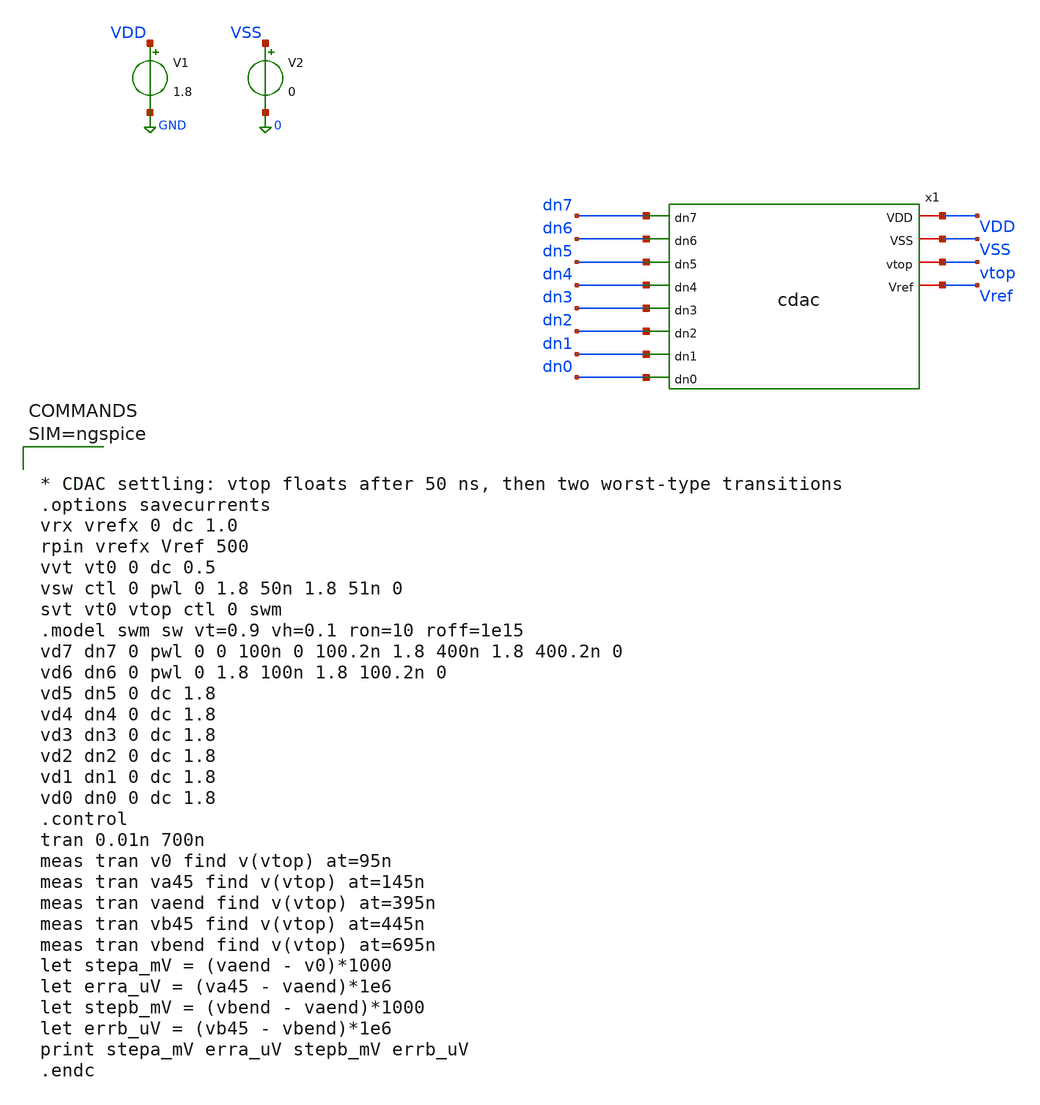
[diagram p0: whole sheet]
** sch_path: xschem/cdac_tb.sch
**.subckt cdac_tb
V1 VDD GND 1.8
V2 VSS 0 0
x1 VDD dn7 dn6 dn5 VSS dn4 dn3 vtop dn2 dn1 Vref dn0 cdac
**** begin user architecture code

** opencircuitdesign pdks install
.lib $::SKYWATER_MODELS/sky130.lib.spice tt




* CDAC settling: vtop floats after 50 ns, then two worst-type transitions
.options savecurrents
vrx vrefx 0 dc 1.0
rpin vrefx Vref 500
vvt vt0 0 dc 0.5
vsw ctl 0 pwl 0 1.8 50n 1.8 51n 0
svt vt0 vtop ctl 0 swm
.model swm sw vt=0.9 vh=0.1 ron=10 roff=1e15
vd7 dn7 0 pwl 0 0 100n 0 100.2n 1.8 400n 1.8 400.2n 0
vd6 dn6 0 pwl 0 1.8 100n 1.8 100.2n 0
vd5 dn5 0 dc 1.8
vd4 dn4 0 dc 1.8
vd3 dn3 0 dc 1.8
vd2 dn2 0 dc 1.8
vd1 dn1 0 dc 1.8
vd0 dn0 0 dc 1.8
.control
tran 0.01n 700n
meas tran v0 find v(vtop) at=95n
meas tran va45 find v(vtop) at=145n
meas tran vaend find v(vtop) at=395n
meas tran vb45 find v(vtop) at=445n
meas tran vbend find v(vtop) at=695n
let stepa_mV = (vaend - v0)*1000
let erra_uV = (va45 - vaend)*1e6
let stepb_mV = (vbend - vaend)*1000
let errb_uV = (vb45 - vbend)*1e6
print stepa_mV erra_uV stepb_mV errb_uV
.endc



**** end user architecture code
**.ends

* expanding   symbol:  cdac.sym # of pins=12
** sym_path: xschem/cdac.sym
** sch_path: xschem/cdac.sch
.subckt cdac VDD dn7 dn6 dn5 VSS dn4 dn3 vtop dn2 dn1 Vref dn0
*.ipin dn7
*.ipin dn6
*.ipin dn5
*.ipin dn4
*.ipin dn3
*.ipin dn2
*.ipin dn1
*.ipin dn0
*.iopin VDD
*.iopin VSS
*.iopin vtop
*.iopin Vref
XMN7 b7 dn7 VSS VSS sky130_fd_pr__nfet_01v8 L=0.15 W=2 nf=1 ad='int((1 + 1)/2) * 2 / 1 * 0.29' as='int((1 + 2)/2) * 2 / 1 * 0.29'
+ pd='2*int((1 + 1)/2) * (2 / 1 + 0.29)' ps='2*int((1 + 2)/2) * (2 / 1 + 0.29)' nrd='0.29 / 2 ' nrs='0.29 / 2 '
+ sa=0 sb=0 sd=0 mult=1 m=1
XMP7 b7 dn7 Vref Vref sky130_fd_pr__pfet_01v8_lvt L=0.35 W=4 nf=1 ad='int((1 + 1)/2) * 4 / 1 * 0.29'
+ as='int((1 + 2)/2) * 4 / 1 * 0.29' pd='2*int((1 + 1)/2) * (4 / 1 + 0.29)' ps='2*int((1 + 2)/2) * (4 / 1 + 0.29)'
+ nrd='0.29 / 4 ' nrs='0.29 / 4 ' sa=0 sb=0 sd=0 mult=1 m=1
XC7 vtop b7 sky130_fd_pr__cap_mim_m3_1 W=1.8 L=1.8 MF=128 m=128
XMN6 b6 dn6 VSS VSS sky130_fd_pr__nfet_01v8 L=0.15 W=1 nf=1 ad='int((1 + 1)/2) * 1 / 1 * 0.29' as='int((1 + 2)/2) * 1 / 1 * 0.29'
+ pd='2*int((1 + 1)/2) * (1 / 1 + 0.29)' ps='2*int((1 + 2)/2) * (1 / 1 + 0.29)' nrd='0.29 / 1 ' nrs='0.29 / 1 '
+ sa=0 sb=0 sd=0 mult=1 m=1
XMP6 b6 dn6 Vref Vref sky130_fd_pr__pfet_01v8_lvt L=0.35 W=2 nf=1 ad='int((1 + 1)/2) * 2 / 1 * 0.29'
+ as='int((1 + 2)/2) * 2 / 1 * 0.29' pd='2*int((1 + 1)/2) * (2 / 1 + 0.29)' ps='2*int((1 + 2)/2) * (2 / 1 + 0.29)'
+ nrd='0.29 / 2 ' nrs='0.29 / 2 ' sa=0 sb=0 sd=0 mult=1 m=1
XC6 vtop b6 sky130_fd_pr__cap_mim_m3_1 W=1.8 L=1.8 MF=64 m=64
XMN5 b5 dn5 VSS VSS sky130_fd_pr__nfet_01v8 L=0.15 W=0.5 nf=1 ad='int((1 + 1)/2) * 0.5 / 1 * 0.29' as='int((1 + 2)/2) * 0.5 / 1 * 0.29'
+ pd='2*int((1 + 1)/2) * (0.5 / 1 + 0.29)' ps='2*int((1 + 2)/2) * (0.5 / 1 + 0.29)' nrd='0.29 / 0.5 ' nrs='0.29 / 0.5 '
+ sa=0 sb=0 sd=0 mult=1 m=1
XMP5 b5 dn5 Vref Vref sky130_fd_pr__pfet_01v8_lvt L=0.35 W=1 nf=1 ad='int((1 + 1)/2) * 1 / 1 * 0.29'
+ as='int((1 + 2)/2) * 1 / 1 * 0.29' pd='2*int((1 + 1)/2) * (1 / 1 + 0.29)' ps='2*int((1 + 2)/2) * (1 / 1 + 0.29)'
+ nrd='0.29 / 1 ' nrs='0.29 / 1 ' sa=0 sb=0 sd=0 mult=1 m=1
XC5 vtop b5 sky130_fd_pr__cap_mim_m3_1 W=1.8 L=1.8 MF=32 m=32
XMN4 b4 dn4 VSS VSS sky130_fd_pr__nfet_01v8 L=0.15 W=0.5 nf=1 ad='int((1 + 1)/2) * 0.5 / 1 * 0.29' as='int((1 + 2)/2) * 0.5 / 1 * 0.29'
+ pd='2*int((1 + 1)/2) * (0.5 / 1 + 0.29)' ps='2*int((1 + 2)/2) * (0.5 / 1 + 0.29)' nrd='0.29 / 0.5 ' nrs='0.29 / 0.5 '
+ sa=0 sb=0 sd=0 mult=1 m=1
XMP4 b4 dn4 Vref Vref sky130_fd_pr__pfet_01v8_lvt L=0.35 W=1 nf=1 ad='int((1 + 1)/2) * 1 / 1 * 0.29'
+ as='int((1 + 2)/2) * 1 / 1 * 0.29' pd='2*int((1 + 1)/2) * (1 / 1 + 0.29)' ps='2*int((1 + 2)/2) * (1 / 1 + 0.29)'
+ nrd='0.29 / 1 ' nrs='0.29 / 1 ' sa=0 sb=0 sd=0 mult=1 m=1
XC4 vtop b4 sky130_fd_pr__cap_mim_m3_1 W=1.8 L=1.8 MF=16 m=16
XMN3 b3 dn3 VSS VSS sky130_fd_pr__nfet_01v8 L=0.15 W=0.5 nf=1 ad='int((1 + 1)/2) * 0.5 / 1 * 0.29' as='int((1 + 2)/2) * 0.5 / 1 * 0.29'
+ pd='2*int((1 + 1)/2) * (0.5 / 1 + 0.29)' ps='2*int((1 + 2)/2) * (0.5 / 1 + 0.29)' nrd='0.29 / 0.5 ' nrs='0.29 / 0.5 '
+ sa=0 sb=0 sd=0 mult=1 m=1
XMP3 b3 dn3 Vref Vref sky130_fd_pr__pfet_01v8_lvt L=0.35 W=1 nf=1 ad='int((1 + 1)/2) * 1 / 1 * 0.29'
+ as='int((1 + 2)/2) * 1 / 1 * 0.29' pd='2*int((1 + 1)/2) * (1 / 1 + 0.29)' ps='2*int((1 + 2)/2) * (1 / 1 + 0.29)'
+ nrd='0.29 / 1 ' nrs='0.29 / 1 ' sa=0 sb=0 sd=0 mult=1 m=1
XC3 vtop b3 sky130_fd_pr__cap_mim_m3_1 W=1.8 L=1.8 MF=8 m=8
XMN2 b2 dn2 VSS VSS sky130_fd_pr__nfet_01v8 L=0.15 W=0.5 nf=1 ad='int((1 + 1)/2) * 0.5 / 1 * 0.29' as='int((1 + 2)/2) * 0.5 / 1 * 0.29'
+ pd='2*int((1 + 1)/2) * (0.5 / 1 + 0.29)' ps='2*int((1 + 2)/2) * (0.5 / 1 + 0.29)' nrd='0.29 / 0.5 ' nrs='0.29 / 0.5 '
+ sa=0 sb=0 sd=0 mult=1 m=1
XMP2 b2 dn2 Vref Vref sky130_fd_pr__pfet_01v8_lvt L=0.35 W=1 nf=1 ad='int((1 + 1)/2) * 1 / 1 * 0.29'
+ as='int((1 + 2)/2) * 1 / 1 * 0.29' pd='2*int((1 + 1)/2) * (1 / 1 + 0.29)' ps='2*int((1 + 2)/2) * (1 / 1 + 0.29)'
+ nrd='0.29 / 1 ' nrs='0.29 / 1 ' sa=0 sb=0 sd=0 mult=1 m=1
XC2 vtop b2 sky130_fd_pr__cap_mim_m3_1 W=1.8 L=1.8 MF=4 m=4
XMN1 b1 dn1 VSS VSS sky130_fd_pr__nfet_01v8 L=0.15 W=0.5 nf=1 ad='int((1 + 1)/2) * 0.5 / 1 * 0.29' as='int((1 + 2)/2) * 0.5 / 1 * 0.29'
+ pd='2*int((1 + 1)/2) * (0.5 / 1 + 0.29)' ps='2*int((1 + 2)/2) * (0.5 / 1 + 0.29)' nrd='0.29 / 0.5 ' nrs='0.29 / 0.5 '
+ sa=0 sb=0 sd=0 mult=1 m=1
XMP1 b1 dn1 Vref Vref sky130_fd_pr__pfet_01v8_lvt L=0.35 W=1 nf=1 ad='int((1 + 1)/2) * 1 / 1 * 0.29'
+ as='int((1 + 2)/2) * 1 / 1 * 0.29' pd='2*int((1 + 1)/2) * (1 / 1 + 0.29)' ps='2*int((1 + 2)/2) * (1 / 1 + 0.29)'
+ nrd='0.29 / 1 ' nrs='0.29 / 1 ' sa=0 sb=0 sd=0 mult=1 m=1
XC1 vtop b1 sky130_fd_pr__cap_mim_m3_1 W=1.8 L=1.8 MF=2 m=2
XMN0 b0 dn0 VSS VSS sky130_fd_pr__nfet_01v8 L=0.15 W=0.5 nf=1 ad='int((1 + 1)/2) * 0.5 / 1 * 0.29' as='int((1 + 2)/2) * 0.5 / 1 * 0.29'
+ pd='2*int((1 + 1)/2) * (0.5 / 1 + 0.29)' ps='2*int((1 + 2)/2) * (0.5 / 1 + 0.29)' nrd='0.29 / 0.5 ' nrs='0.29 / 0.5 '
+ sa=0 sb=0 sd=0 mult=1 m=1
XMP0 b0 dn0 Vref Vref sky130_fd_pr__pfet_01v8_lvt L=0.35 W=1 nf=1 ad='int((1 + 1)/2) * 1 / 1 * 0.29'
+ as='int((1 + 2)/2) * 1 / 1 * 0.29' pd='2*int((1 + 1)/2) * (1 / 1 + 0.29)' ps='2*int((1 + 2)/2) * (1 / 1 + 0.29)'
+ nrd='0.29 / 1 ' nrs='0.29 / 1 ' sa=0 sb=0 sd=0 mult=1 m=1
XC0 vtop b0 sky130_fd_pr__cap_mim_m3_1 W=1.8 L=1.8 MF=1 m=1
XCdmy vtop VSS sky130_fd_pr__cap_mim_m3_1 W=1.8 L=1.8 MF=1 m=1
.ends

.GLOBAL GND
.end
